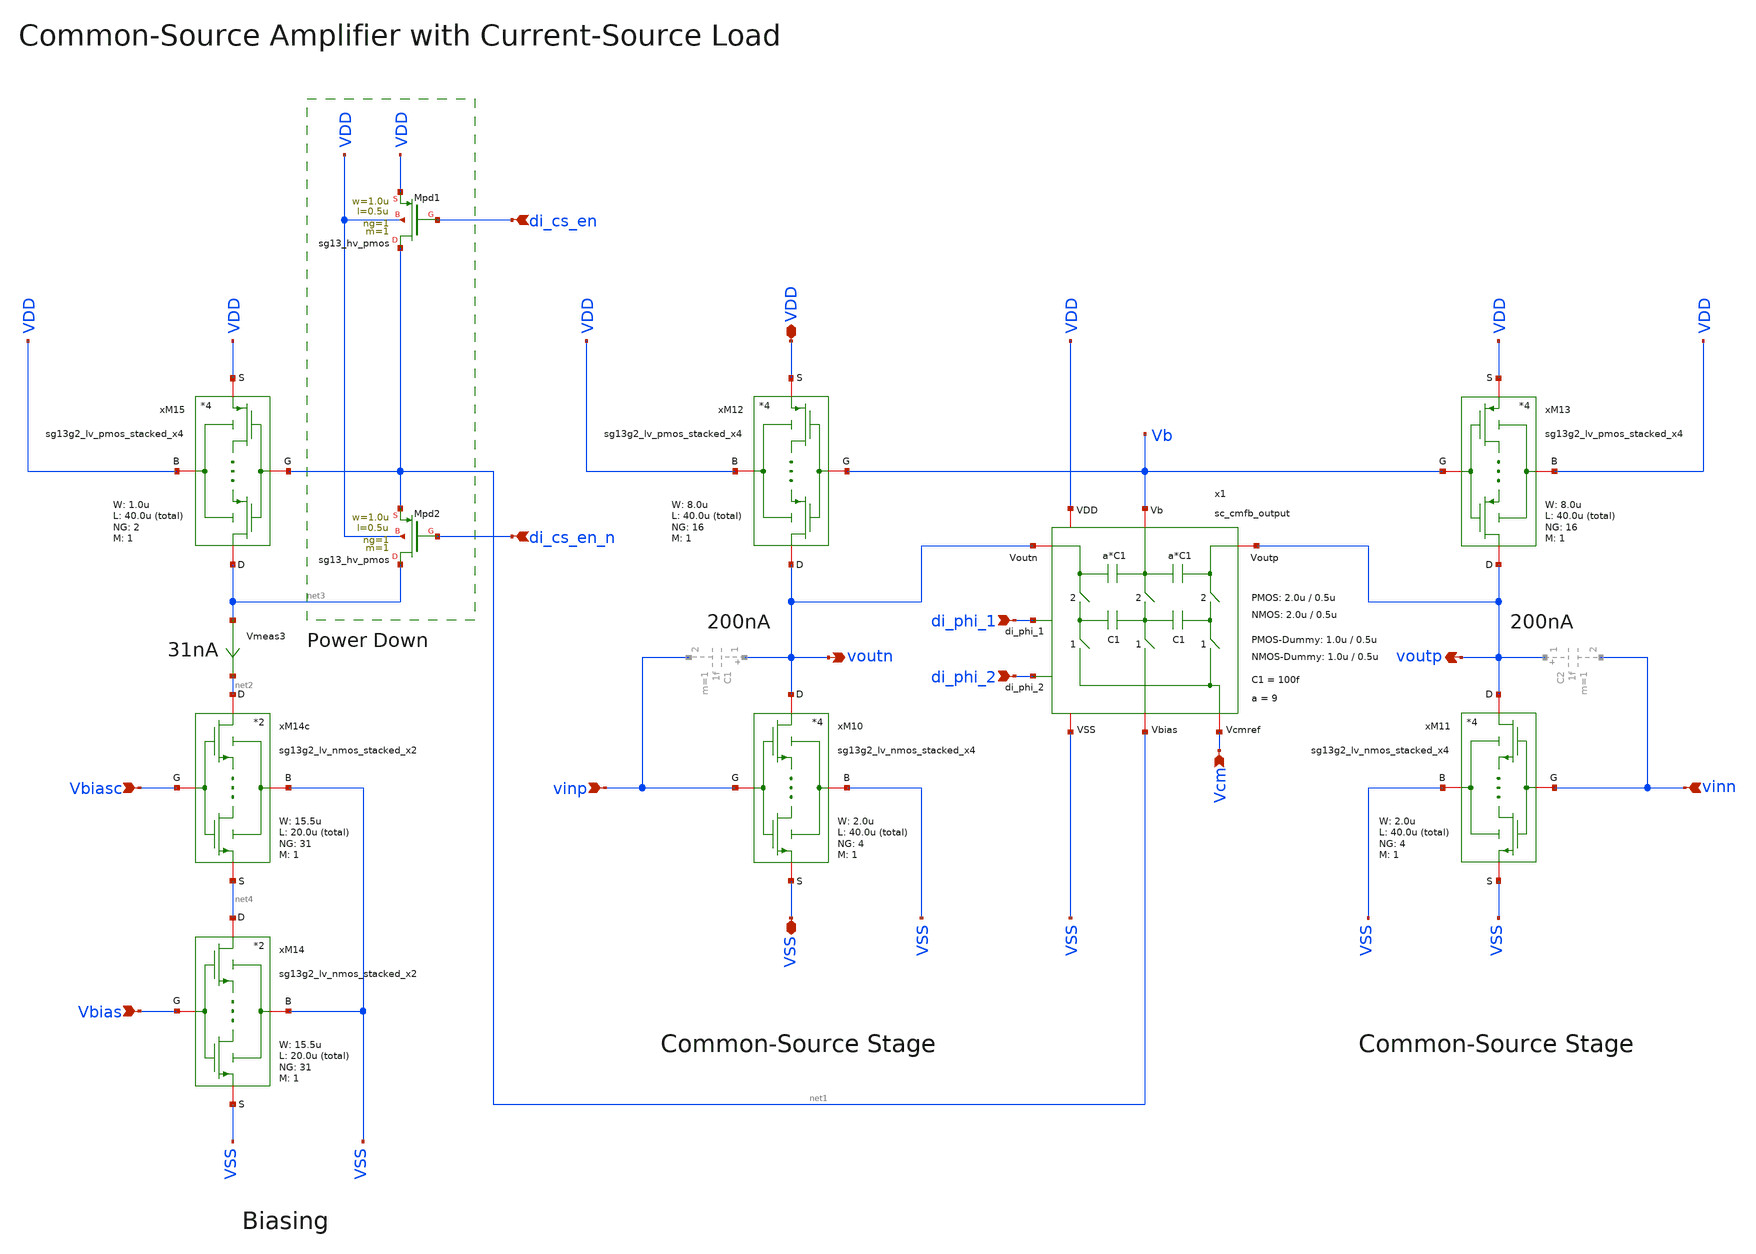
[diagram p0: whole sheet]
** sch_path: SG13G2_ATBS-ADC-main/xschem/bio_amplifier/amplifier_core/common_source_amplifier/common_source_amplifier.sch
**.subckt common_source_amplifier vinp vinn voutp voutn VDD VSS di_phi_1 di_phi_2 Vcm di_cs_en
*+ di_cs_en_n Vbias Vbiasc
*.ipin vinp
*.ipin vinn
*.opin voutp
*.opin voutn
*.iopin VDD
*.iopin VSS
*.ipin di_phi_1
*.ipin di_phi_2
*.ipin Vcm
*.ipin di_cs_en
*.ipin di_cs_en_n
*.ipin Vbias
*.ipin Vbiasc
xM12 voutn Vb VDD VDD sg13g2_lv_pmos_stacked_x4 W_P=8.0u L_P=40.0u NG_P=16 M_P=1
xM10 voutn vinp VSS VSS sg13g2_lv_nmos_stacked_x4 W_N=2.0u L_N=40.0u NG_N=4 M_N=1
xM13 voutp Vb VDD VDD sg13g2_lv_pmos_stacked_x4 W_P=8.0u L_P=40.0u NG_P=16 M_P=1
xM11 voutp vinn VSS VSS sg13g2_lv_nmos_stacked_x4 W_N=2.0u L_N=40.0u NG_N=4 M_N=1
xM15 net3 net1 VDD VDD sg13g2_lv_pmos_stacked_x4 W_P=1.0u L_P=40.0u NG_P=2 M_P=1
x1 Vcm net1 di_phi_1 di_phi_2 VDD voutp VSS Vb voutn sc_cmfb_output W_P_CMFB=2.0u L_P_CMFB=0.5u
+ W_N_CMFB=2.0u L_N_CMFB=0.5u W_P_CMFB_D=1.0u W_N_CMFB_D=1.0u C1=100f a=9
xM14c net2 Vbiasc VSS net4 sg13g2_lv_nmos_stacked_x2 W_N=15.5u L_N=20.0u NG_N=31 M_N=1
Vmeas3 net3 net2 0
.save i(vmeas3)
XMpd2 net3 di_cs_en_n net1 VDD sg13_hv_pmos w=1.0u l=0.5u ng=1 m=1 mm_ok=1
XMpd1 net1 di_cs_en VDD VDD sg13_hv_pmos w=1.0u l=0.5u ng=1 m=1 mm_ok=1
xM14 net4 Vbias VSS VSS sg13g2_lv_nmos_stacked_x2 W_N=15.5u L_N=20.0u NG_N=31 M_N=1
**.ends

* expanding   symbol:  stacked_transistors/sg13g2_lv_pmos_stacked/sg13g2_lv_pmos_stacked_x4.sym # of
*+ pins=4
** sym_path: SG13G2_ATBS-ADC-main/xschem/stacked_transistors/sg13g2_lv_pmos_stacked/sg13g2_lv_pmos_stacked_x4.sym
** sch_path: SG13G2_ATBS-ADC-main/xschem/stacked_transistors/sg13g2_lv_pmos_stacked/sg13g2_lv_pmos_stacked_x4.sch
.subckt sg13g2_lv_pmos_stacked_x4 D G B S  W_P=1.0u L_P=0.45u NG_P=1 M_P=1
*.iopin D
*.iopin S
*.iopin G
*.iopin B
XM1 net1 G S B sg13_lv_pmos w=W_P l=L_P/4 ng=NG_P m=M_P mm_ok=1
XM2 net3 G net1 B sg13_lv_pmos w=W_P l=L_P/4 ng=NG_P m=M_P mm_ok=1
XM3 net2 G net3 B sg13_lv_pmos w=W_P l=L_P/4 ng=NG_P m=M_P mm_ok=1
XM4 D G net2 B sg13_lv_pmos w=W_P l=L_P/4 ng=NG_P m=M_P mm_ok=1
.ends


* expanding   symbol:  stacked_transistors/sg13g2_lv_nmos_stacked/sg13g2_lv_nmos_stacked_x4.sym # of
*+ pins=4
** sym_path: SG13G2_ATBS-ADC-main/xschem/stacked_transistors/sg13g2_lv_nmos_stacked/sg13g2_lv_nmos_stacked_x4.sym
** sch_path: SG13G2_ATBS-ADC-main/xschem/stacked_transistors/sg13g2_lv_nmos_stacked/sg13g2_lv_nmos_stacked_x4.sch
.subckt sg13g2_lv_nmos_stacked_x4 D G B S  W_N=1.0u L_N=0.45u NG_N=1 M_N=1
*.iopin D
*.iopin S
*.iopin G
*.iopin B
XM1 net1 G S B sg13_lv_nmos w=W_N l=L_N/4 ng=NG_N m=M_N mm_ok=1
XM2 net3 G net1 B sg13_lv_nmos w=W_N l=L_N/4 ng=NG_N m=M_N mm_ok=1
XM3 net2 G net3 B sg13_lv_nmos w=W_N l=L_N/4 ng=NG_N m=M_N mm_ok=1
XM4 D G net2 B sg13_lv_nmos w=W_N l=L_N/4 ng=NG_N m=M_N mm_ok=1
.ends


* expanding   symbol:  bio_amplifier/amplifier_core/sc_cmfb/sc_cmfb_output.sym # of pins=9
** sym_path: SG13G2_ATBS-ADC-main/xschem/bio_amplifier/amplifier_core/sc_cmfb/sc_cmfb_output.sym
** sch_path: SG13G2_ATBS-ADC-main/xschem/bio_amplifier/amplifier_core/sc_cmfb/sc_cmfb_output.sch
.subckt sc_cmfb_output Vcmref Vbias di_phi_1 di_phi_2 VDD Voutp VSS Vb Voutn  W_P_CMFB=2.0u
+ L_P_CMFB=0.5u W_N_CMFB=2.0u L_N_CMFB=0.5u W_P_CMFB_D=1.0u W_N_CMFB_D=1.0u C1=100f a=9
*.iopin VSS
*.iopin VDD
*.iopin Vb
*.iopin Voutp
*.iopin Voutn
*.iopin Vbias
*.iopin Vcmref
*.ipin di_phi_1
*.ipin di_phi_2
x1 VDD di_phi_2 VSS net1 Voutp di_phi_2_n transmission_gate_lv_wo_dummy W_P=W_P_CMFB L_P=L_P_CMFB
+ W_N=W_N_CMFB L_N=L_N_CMFB
C1 Voutp Vb {a*C1} m=1
x2 VDD di_phi_2 VSS net3 Vb di_phi_2_n transmission_gate_lv_wo_dummy W_P=W_P_CMFB L_P=L_P_CMFB
+ W_N=W_N_CMFB L_N=L_N_CMFB
x3 VDD di_phi_2 VSS net2 Voutn di_phi_2_n transmission_gate_lv_wo_dummy W_P=W_P_CMFB L_P=L_P_CMFB
+ W_N=W_N_CMFB L_N=L_N_CMFB
C2 Vb Voutn {a*C1} m=1
C3 net1 net3 C1 m=1
C4 net3 net2 C1 m=1
x7 VDD di_phi_1 di_phi_1_n VSS inverter_lv W_P=W_P_CMFB/2 L_P=L_P_CMFB W_N=W_N_CMFB/2 L_N=L_N_CMFB
x8 VDD di_phi_2 di_phi_2_n VSS inverter_lv W_P=W_P_CMFB/2 L_P=L_P_CMFB W_N=W_N_CMFB/2 L_N=L_N_CMFB
x4 VDD di_phi_1 VSS Vcmref net1 di_phi_1_n transmission_gate_lv_w_dummy W_P=W_P_CMFB L_P=L_P_CMFB
+ W_N=W_N_CMFB L_N=L_N_CMFB W_P_D=W_P_CMFB_D L_P_D=L_P_CMFB W_N_D=W_N_CMFB_D L_N_D=L_N_CMFB
x5 VDD di_phi_1 VSS Vbias net3 di_phi_1_n transmission_gate_lv_w_dummy W_P=W_P_CMFB L_P=L_P_CMFB
+ W_N=W_N_CMFB L_N=L_N_CMFB W_P_D=W_P_CMFB_D L_P_D=L_P_CMFB W_N_D=W_N_CMFB_D L_N_D=L_N_CMFB
x6 VDD di_phi_1 VSS Vcmref net2 di_phi_1_n transmission_gate_lv_w_dummy W_P=W_P_CMFB L_P=L_P_CMFB
+ W_N=W_N_CMFB L_N=L_N_CMFB W_P_D=W_P_CMFB_D L_P_D=L_P_CMFB W_N_D=W_N_CMFB_D L_N_D=L_N_CMFB
.ends


* expanding   symbol:  stacked_transistors/sg13g2_lv_nmos_stacked/sg13g2_lv_nmos_stacked_x2.sym # of
*+ pins=4
** sym_path: SG13G2_ATBS-ADC-main/xschem/stacked_transistors/sg13g2_lv_nmos_stacked/sg13g2_lv_nmos_stacked_x2.sym
** sch_path: SG13G2_ATBS-ADC-main/xschem/stacked_transistors/sg13g2_lv_nmos_stacked/sg13g2_lv_nmos_stacked_x2.sch
.subckt sg13g2_lv_nmos_stacked_x2 D G B S  W_N=1.0u L_N=0.45u NG_N=1 M_N=1
*.iopin D
*.iopin S
*.iopin G
*.iopin B
XM1 net1 G S B sg13_lv_nmos w=W_N l=L_N/2 ng=NG_N m=M_N mm_ok=1
XM2 D G net1 B sg13_lv_nmos w=W_N l=L_N/2 ng=NG_N m=M_N mm_ok=1
.ends


* expanding   symbol:  transmission_gate/transmission_gate_lv_wo_dummy.sym # of pins=6
** sym_path: SG13G2_ATBS-ADC-main/xschem/transmission_gate/transmission_gate_lv_wo_dummy.sym
** sch_path: SG13G2_ATBS-ADC-main/xschem/transmission_gate/transmission_gate_lv_wo_dummy.sch
.subckt transmission_gate_lv_wo_dummy VDD di_tg_ctrl VSS v_b v_a di_tg_ctrl_n  W_P=1.0u L_P=0.13u
+ W_N=1.0u L_N=0.13u
*.iopin v_a
*.iopin v_b
*.iopin VDD
*.iopin VSS
*.ipin di_tg_ctrl
*.ipin di_tg_ctrl_n
XM1 v_a di_tg_ctrl v_b VSS sg13_lv_nmos w=W_N l=L_N ng=1 m=1 mm_ok=1
XM2 v_a di_tg_ctrl_n v_b VDD sg13_lv_pmos w=W_P l=L_P ng=1 m=1 mm_ok=1
.ends


* expanding   symbol:  inverter/inverter_lv.sym # of pins=4
** sym_path: SG13G2_ATBS-ADC-main/xschem/inverter/inverter_lv.sym
** sch_path: SG13G2_ATBS-ADC-main/xschem/inverter/inverter_lv.sch
.subckt inverter_lv VDD vin vout VSS  W_P=3.0u L_P=0.13u W_N=1.0u L_N=0.13u
*.ipin vin
*.iopin VDD
*.iopin VSS
*.opin vout
XM1 vout vin VDD VDD sg13_lv_pmos w=W_P l=L_P ng=1 m=1 mm_ok=1
XM2 vout vin VSS VSS sg13_lv_nmos w=W_N l=L_N ng=1 m=1 mm_ok=1
.ends


* expanding   symbol:  transmission_gate/transmission_gate_lv_w_dummy.sym # of pins=6
** sym_path: SG13G2_ATBS-ADC-main/xschem/transmission_gate/transmission_gate_lv_w_dummy.sym
** sch_path: SG13G2_ATBS-ADC-main/xschem/transmission_gate/transmission_gate_lv_w_dummy.sch
.subckt transmission_gate_lv_w_dummy VDD di_tg_ctrl VSS v_b v_a di_tg_ctrl_n  W_P=2.0u L_P=0.13u
+ W_N=2.0u L_N=0.13u W_P_D=1.0u L_P_D=0.13u W_N_D=1.0u L_N_D=0.13u
*.iopin v_a
*.iopin v_b
*.iopin VDD
*.iopin VSS
*.ipin di_tg_ctrl
*.ipin di_tg_ctrl_n
XM1 v_a di_tg_ctrl v_b VSS sg13_lv_nmos w=W_N l=L_N ng=1 m=1 mm_ok=1
XM2 v_a di_tg_ctrl_n v_b VDD sg13_lv_pmos w=W_P l=L_P ng=1 m=1 mm_ok=1
XMdummy2 v_b di_tg_ctrl v_b VDD sg13_lv_pmos w=W_P_D l=L_P_D ng=1 m=1 mm_ok=1
XMdummy1 v_b di_tg_ctrl_n v_b VSS sg13_lv_nmos w=W_N_D l=L_N_D ng=1 m=1 mm_ok=1
.ends

.end
